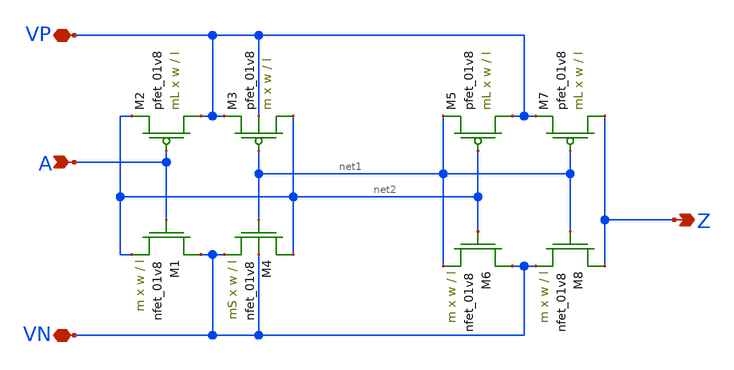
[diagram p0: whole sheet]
** sch_path: schematics/inverter_schmitt_lvs.sch
**.subckt inverter_schmitt_lvs A VP VN Z
*.ipin A
*.iopin VP
*.iopin VN
*.opin Z
XM1 VN A net2 GND sky130_fd_pr__nfet_01v8 L=l W=w nf=1 ad='int((nf+1)/2) * W/nf * 0.29' as='int((nf+2)/2) * W/nf * 0.29'
+ pd='2*int((nf+1)/2) * (W/nf + 0.29)' ps='2*int((nf+2)/2) * (W/nf + 0.29)' nrd='0.29 / W' nrs='0.29 / W'
+ sa=0 sb=0 sd=0 mult=m m=m
XM2 VP A net2 VDD sky130_fd_pr__pfet_01v8 L=l W=w nf=1 ad='int((nf+1)/2) * W/nf * 0.29' as='int((nf+2)/2) * W/nf * 0.29'
+ pd='2*int((nf+1)/2) * (W/nf + 0.29)' ps='2*int((nf+2)/2) * (W/nf + 0.29)' nrd='0.29 / W' nrs='0.29 / W'
+ sa=0 sb=0 sd=0 mult=mL m=mL
XM5 VP net2 net1 VDD sky130_fd_pr__pfet_01v8 L=l W=w nf=1 ad='int((nf+1)/2) * W/nf * 0.29' as='int((nf+2)/2) * W/nf * 0.29'
+ pd='2*int((nf+1)/2) * (W/nf + 0.29)' ps='2*int((nf+2)/2) * (W/nf + 0.29)' nrd='0.29 / W' nrs='0.29 / W'
+ sa=0 sb=0 sd=0 mult=mL m=mL
XM6 VN net2 net1 GND sky130_fd_pr__nfet_01v8 L=l W=w nf=1 ad='int((nf+1)/2) * W/nf * 0.29' as='int((nf+2)/2) * W/nf * 0.29'
+ pd='2*int((nf+1)/2) * (W/nf + 0.29)' ps='2*int((nf+2)/2) * (W/nf + 0.29)' nrd='0.29 / W' nrs='0.29 / W'
+ sa=0 sb=0 sd=0 mult=m m=m
XM3 net2 net1 VP VP sky130_fd_pr__pfet_01v8 L=l W=w nf=1 ad='int((nf+1)/2) * W/nf * 0.29' as='int((nf+2)/2) * W/nf * 0.29'
+ pd='2*int((nf+1)/2) * (W/nf + 0.29)' ps='2*int((nf+2)/2) * (W/nf + 0.29)' nrd='0.29 / W' nrs='0.29 / W'
+ sa=0 sb=0 sd=0 mult=m m=m
XM4 net2 net1 VN VN sky130_fd_pr__nfet_01v8 L=l W=w nf=1 ad='int((nf+1)/2) * W/nf * 0.29' as='int((nf+2)/2) * W/nf * 0.29'
+ pd='2*int((nf+1)/2) * (W/nf + 0.29)' ps='2*int((nf+2)/2) * (W/nf + 0.29)' nrd='0.29 / W' nrs='0.29 / W'
+ sa=0 sb=0 sd=0 mult=mS m=mS
XM7 Z net1 VP VDD sky130_fd_pr__pfet_01v8 L=l W=w nf=1 ad='int((nf+1)/2) * W/nf * 0.29' as='int((nf+2)/2) * W/nf * 0.29'
+ pd='2*int((nf+1)/2) * (W/nf + 0.29)' ps='2*int((nf+2)/2) * (W/nf + 0.29)' nrd='0.29 / W' nrs='0.29 / W'
+ sa=0 sb=0 sd=0 mult=mL m=mL
XM8 Z net1 VN GND sky130_fd_pr__nfet_01v8 L=l W=w nf=1 ad='int((nf+1)/2) * W/nf * 0.29' as='int((nf+2)/2) * W/nf * 0.29'
+ pd='2*int((nf+1)/2) * (W/nf + 0.29)' ps='2*int((nf+2)/2) * (W/nf + 0.29)' nrd='0.29 / W' nrs='0.29 / W'
+ sa=0 sb=0 sd=0 mult=m m=m
**.ends
.end
